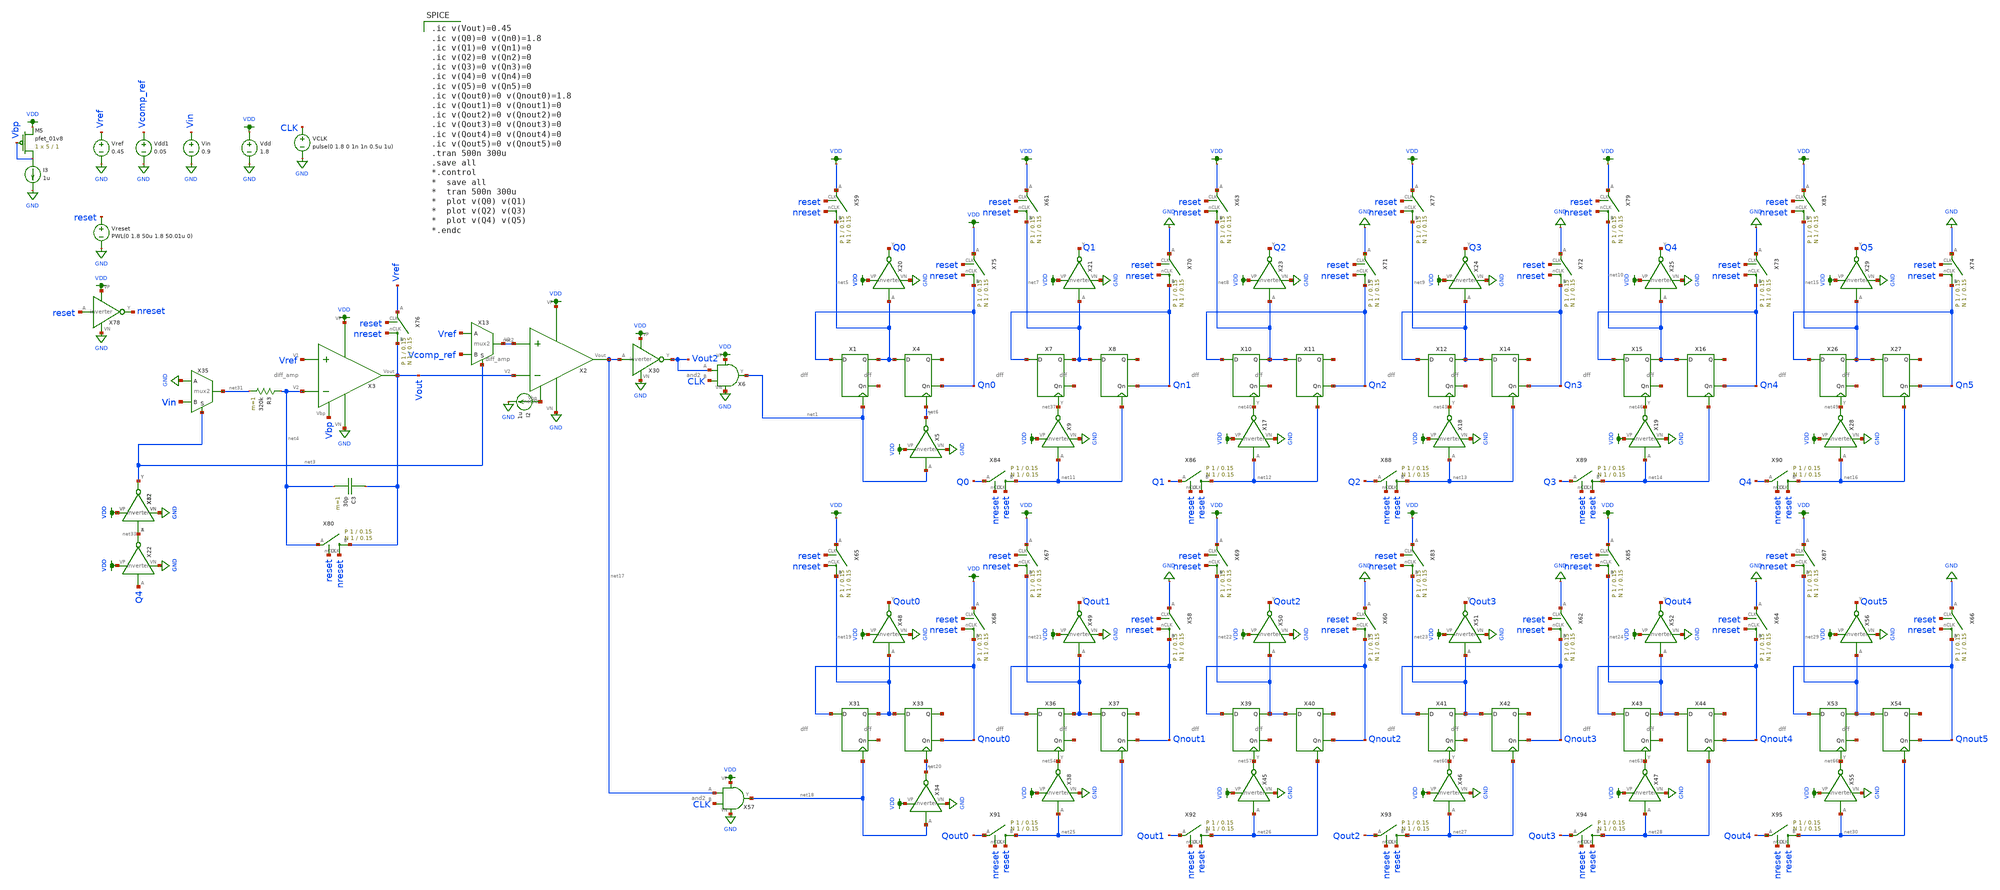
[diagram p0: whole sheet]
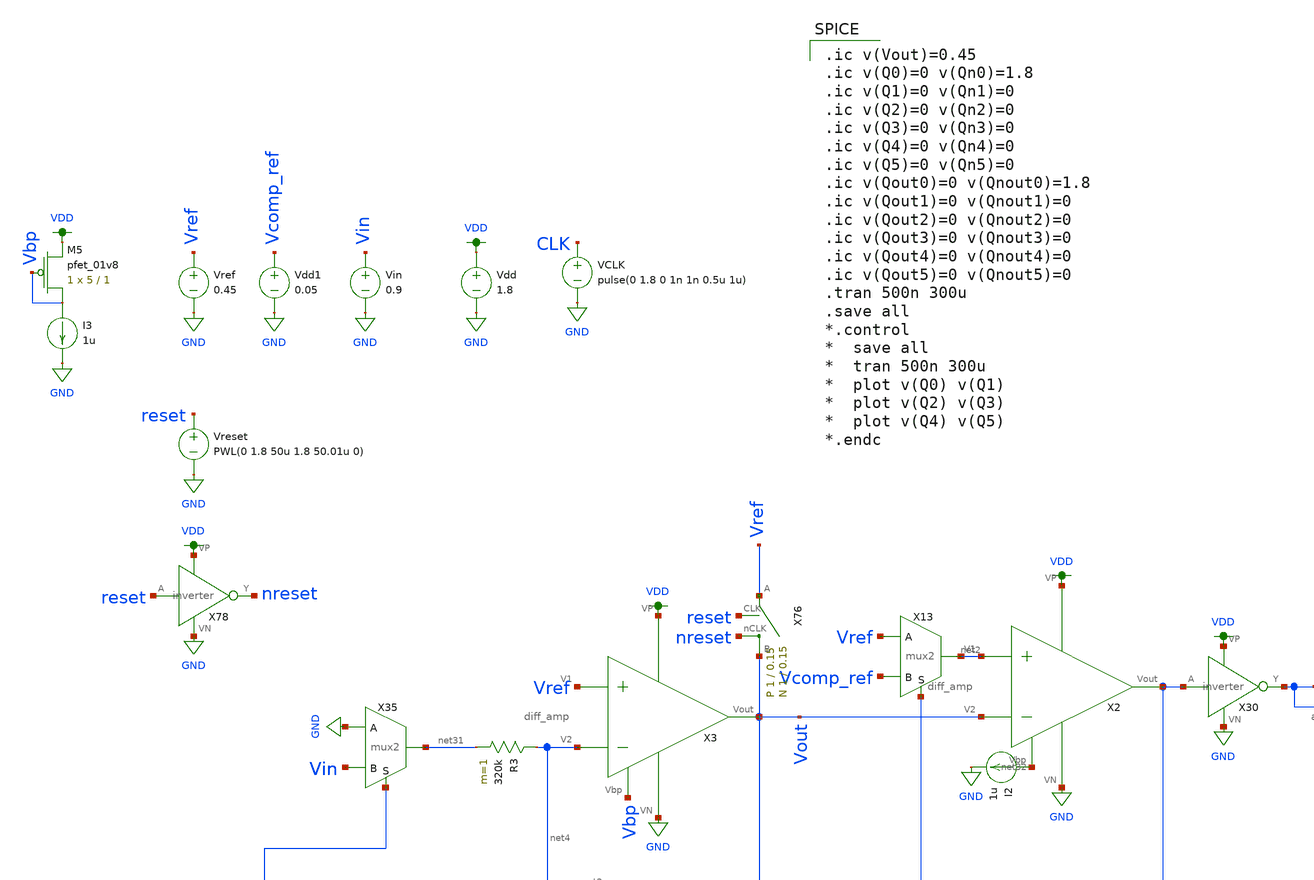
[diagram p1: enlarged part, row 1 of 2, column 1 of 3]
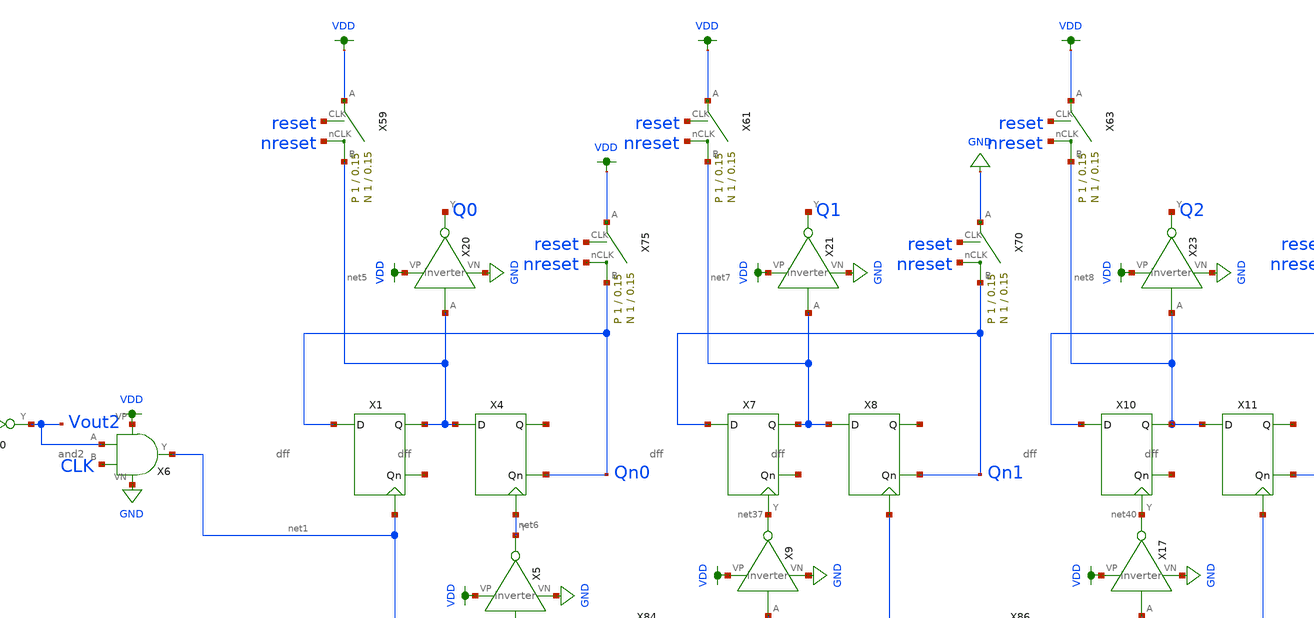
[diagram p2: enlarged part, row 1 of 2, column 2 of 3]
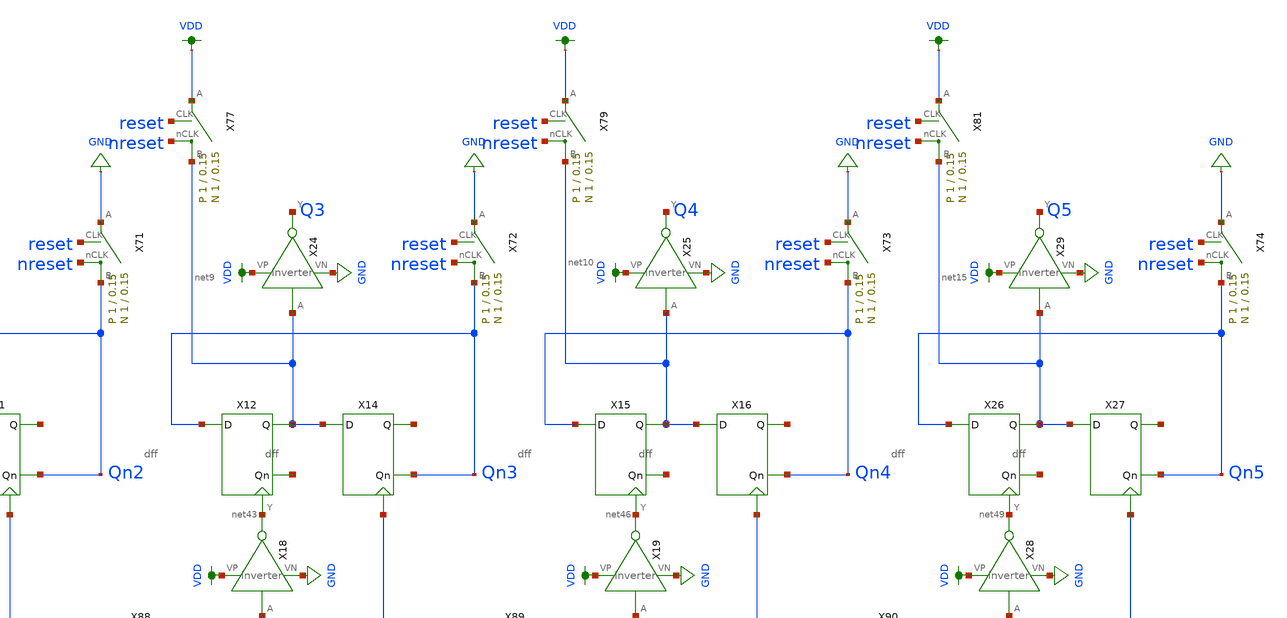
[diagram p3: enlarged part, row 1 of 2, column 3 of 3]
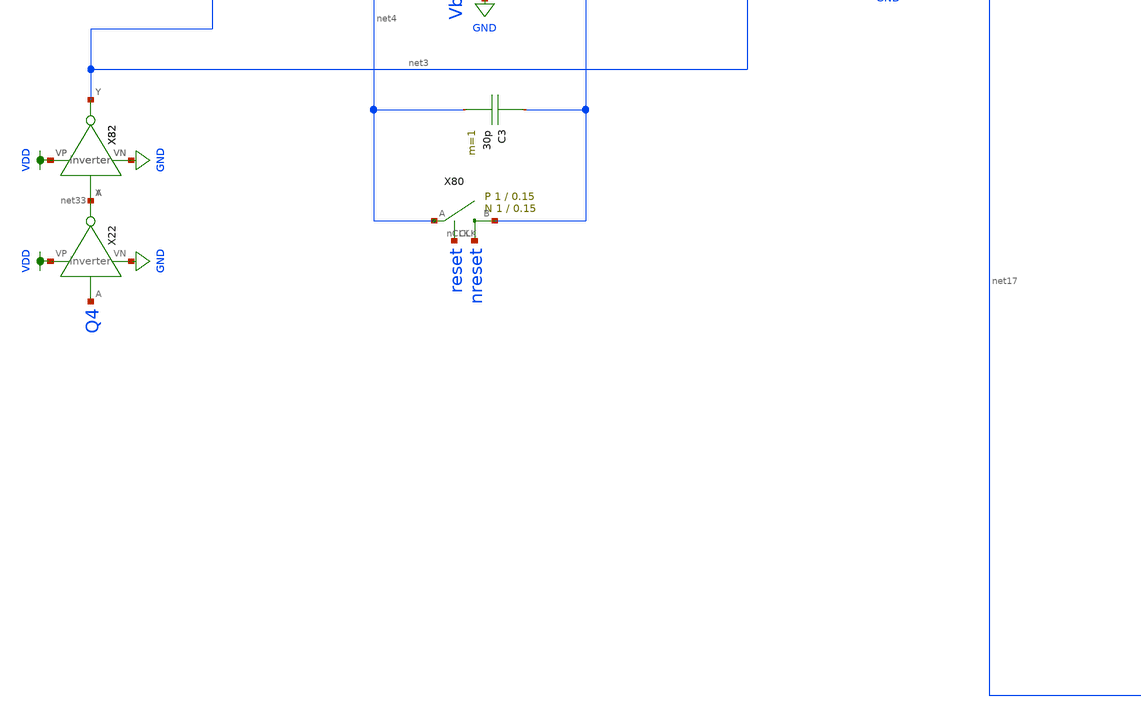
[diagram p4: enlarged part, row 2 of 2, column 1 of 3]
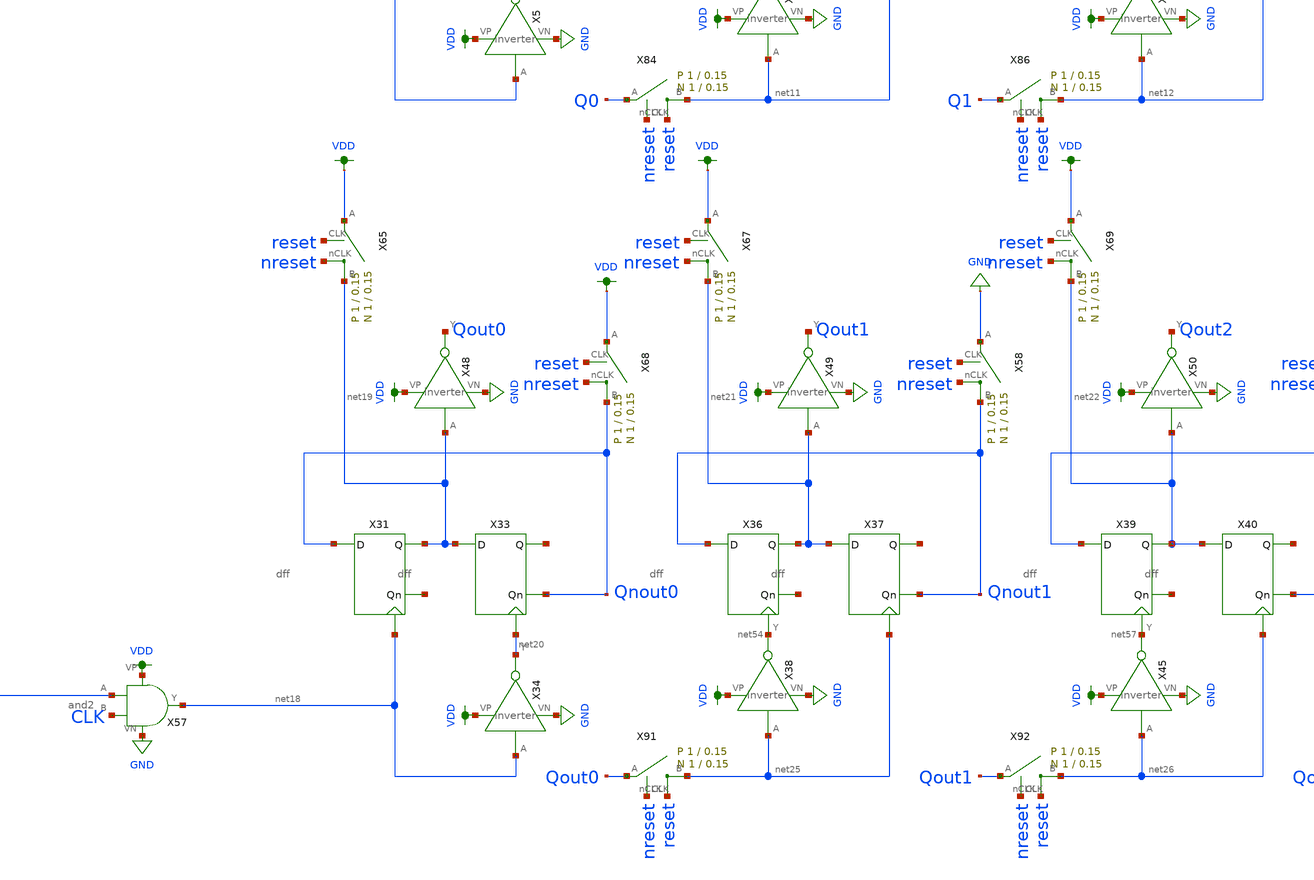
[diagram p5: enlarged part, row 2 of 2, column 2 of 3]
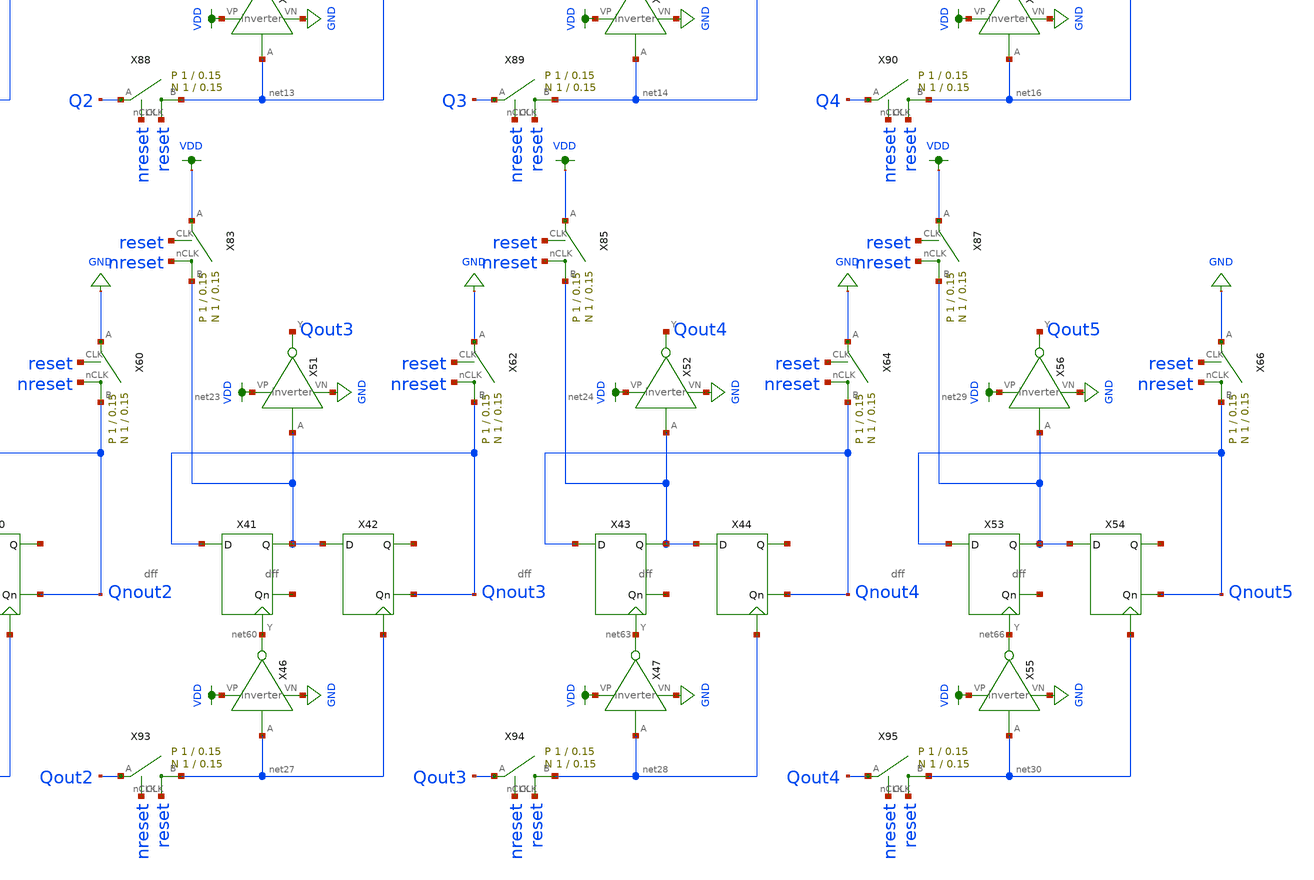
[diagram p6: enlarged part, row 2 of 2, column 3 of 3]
** sch_path: schematic/archive/double-slope-works.sch
**.subckt double-slope-works
X2 VDD net32 net17 net2 Vout GND diff_amp
Vdd VDD GND 1.8
VCLK CLK GND pulse(0 1.8 0 1n 1n 0.5u 1u)
Vdd1 Vcomp_ref GND 0.05
Vin Vin GND 0.9
I2 net32 GND 1u
X6 VDD Vout2 GND net1 CLK and2
X13 net2 Vref Vcomp_ref net3 mux2
X22 Q4 net33 VDD GND inverter
X32 net33 net3 VDD GND inverter
X35 net31 GND Vin net3 mux2
XM5 Vbp Vbp VDD VDD sky130_fd_pr__pfet_01v8 L=1 W=5 nf=1 ad='int((nf+1)/2) * W/nf * 0.29' as='int((nf+2)/2) * W/nf * 0.29'
+ pd='2*int((nf+1)/2) * (W/nf + 0.29)' ps='2*int((nf+2)/2) * (W/nf + 0.29)' nrd='0.29 / W' nrs='0.29 / W'
+ sa=0 sb=0 sd=0 mult=1 m=1
I3 Vbp GND 1u
C3 Vout net4 30p m=1
X3 VDD Vbp Vout Vref net4 GND diff_amp
R3 net4 net31 320k m=1
Vref Vref GND 0.45
X1 Qn0 net34 net5 net1 dff
X4 net5 Qn0 net35 net6 dff
X5 net1 net6 VDD GND inverter
X7 Qn1 net36 net7 net37 dff
X8 net7 Qn1 net38 net11 dff
X9 net11 net37 VDD GND inverter
X10 Qn2 net39 net8 net40 dff
X11 net8 Qn2 net41 net12 dff
X12 Qn3 net42 net9 net43 dff
X14 net9 Qn3 net44 net13 dff
X15 Qn4 net45 net10 net46 dff
X16 net10 Qn4 net47 net14 dff
X17 net12 net40 VDD GND inverter
X18 net13 net43 VDD GND inverter
X19 net14 net46 VDD GND inverter
X20 net5 Q0 VDD GND inverter
X21 net7 Q1 VDD GND inverter
X23 net8 Q2 VDD GND inverter
X24 net9 Q3 VDD GND inverter
X25 net10 Q4 VDD GND inverter
X26 Qn5 net48 net15 net49 dff
X27 net15 Qn5 net50 net16 dff
X28 net16 net49 VDD GND inverter
X29 net15 Q5 VDD GND inverter
X30 net17 Vout2 VDD GND inverter
X31 Qnout0 net51 net19 net18 dff
X33 net19 Qnout0 net52 net20 dff
X34 net18 net20 VDD GND inverter
X36 Qnout1 net53 net21 net54 dff
X37 net21 Qnout1 net55 net25 dff
X38 net25 net54 VDD GND inverter
X39 Qnout2 net56 net22 net57 dff
X40 net22 Qnout2 net58 net26 dff
X41 Qnout3 net59 net23 net60 dff
X42 net23 Qnout3 net61 net27 dff
X43 Qnout4 net62 net24 net63 dff
X44 net24 Qnout4 net64 net28 dff
X45 net26 net57 VDD GND inverter
X46 net27 net60 VDD GND inverter
X47 net28 net63 VDD GND inverter
X48 net19 Qout0 VDD GND inverter
X49 net21 Qout1 VDD GND inverter
X50 net22 Qout2 VDD GND inverter
X51 net23 Qout3 VDD GND inverter
X52 net24 Qout4 VDD GND inverter
X53 Qnout5 net65 net29 net66 dff
X54 net29 Qnout5 net67 net30 dff
X55 net30 net66 VDD GND inverter
X56 net29 Qout5 VDD GND inverter
X57 VDD net17 GND net18 CLK and2
X70 Qn1 GND reset nreset switch Wp=1 Lp=0.15 WW=1 LL=0.15
X71 Qn2 GND reset nreset switch Wp=1 Lp=0.15 WW=1 LL=0.15
X72 Qn3 GND reset nreset switch Wp=1 Lp=0.15 WW=1 LL=0.15
X73 Qn4 GND reset nreset switch Wp=1 Lp=0.15 WW=1 LL=0.15
X74 Qn5 GND reset nreset switch Wp=1 Lp=0.15 WW=1 LL=0.15
X75 Qn0 VDD reset nreset switch Wp=1 Lp=0.15 WW=1 LL=0.15
X59 net5 VDD reset nreset switch Wp=1 Lp=0.15 WW=1 LL=0.15
X61 net7 VDD reset nreset switch Wp=1 Lp=0.15 WW=1 LL=0.15
X63 net8 VDD reset nreset switch Wp=1 Lp=0.15 WW=1 LL=0.15
X77 net9 VDD reset nreset switch Wp=1 Lp=0.15 WW=1 LL=0.15
X79 net10 VDD reset nreset switch Wp=1 Lp=0.15 WW=1 LL=0.15
X81 net15 VDD reset nreset switch Wp=1 Lp=0.15 WW=1 LL=0.15
X65 net19 VDD reset nreset switch Wp=1 Lp=0.15 WW=1 LL=0.15
X67 net21 VDD reset nreset switch Wp=1 Lp=0.15 WW=1 LL=0.15
X69 net22 VDD reset nreset switch Wp=1 Lp=0.15 WW=1 LL=0.15
X83 net23 VDD reset nreset switch Wp=1 Lp=0.15 WW=1 LL=0.15
X85 net24 VDD reset nreset switch Wp=1 Lp=0.15 WW=1 LL=0.15
X87 net29 VDD reset nreset switch Wp=1 Lp=0.15 WW=1 LL=0.15
X58 Qnout1 GND reset nreset switch Wp=1 Lp=0.15 WW=1 LL=0.15
X60 Qnout2 GND reset nreset switch Wp=1 Lp=0.15 WW=1 LL=0.15
X62 Qnout3 GND reset nreset switch Wp=1 Lp=0.15 WW=1 LL=0.15
X64 Qnout4 GND reset nreset switch Wp=1 Lp=0.15 WW=1 LL=0.15
X66 Qnout5 GND reset nreset switch Wp=1 Lp=0.15 WW=1 LL=0.15
X68 Qnout0 VDD reset nreset switch Wp=1 Lp=0.15 WW=1 LL=0.15
X76 Vout Vref reset nreset switch Wp=1 Lp=0.15 WW=1 LL=0.15
Vreset reset GND PWL(0 1.8 50u 1.8 50.01u 0)
X78 reset nreset VDD GND inverter
X80 Vout net4 reset nreset switch Wp=1 Lp=0.15 WW=1 LL=0.15
X82 net33 net3 VDD GND inverter
X84 net11 Q0 nreset reset switch Wp=1 Lp=0.15 WW=1 LL=0.15
X86 net12 Q1 nreset reset switch Wp=1 Lp=0.15 WW=1 LL=0.15
X88 net13 Q2 nreset reset switch Wp=1 Lp=0.15 WW=1 LL=0.15
X89 net14 Q3 nreset reset switch Wp=1 Lp=0.15 WW=1 LL=0.15
X90 net16 Q4 nreset reset switch Wp=1 Lp=0.15 WW=1 LL=0.15
X91 net25 Qout0 nreset reset switch Wp=1 Lp=0.15 WW=1 LL=0.15
X92 net26 Qout1 nreset reset switch Wp=1 Lp=0.15 WW=1 LL=0.15
X93 net27 Qout2 nreset reset switch Wp=1 Lp=0.15 WW=1 LL=0.15
X94 net28 Qout3 nreset reset switch Wp=1 Lp=0.15 WW=1 LL=0.15
X95 net30 Qout4 nreset reset switch Wp=1 Lp=0.15 WW=1 LL=0.15
**** begin user architecture code

.ic v(Vout)=0.45
.ic v(Q0)=0 v(Qn0)=1.8
.ic v(Q1)=0 v(Qn1)=0
.ic v(Q2)=0 v(Qn2)=0
.ic v(Q3)=0 v(Qn3)=0
.ic v(Q4)=0 v(Qn4)=0
.ic v(Q5)=0 v(Qn5)=0
.ic v(Qout0)=0 v(Qnout0)=1.8
.ic v(Qout1)=0 v(Qnout1)=0
.ic v(Qout2)=0 v(Qnout2)=0
.ic v(Qout3)=0 v(Qnout3)=0
.ic v(Qout4)=0 v(Qnout4)=0
.ic v(Qout5)=0 v(Qnout5)=0
.tran 500n 300u
.save all
*.control
*  save all
*  tran 500n 300u
*  plot v(Q0) v(Q1)
*  plot v(Q2) v(Q3)
*  plot v(Q4) v(Q5)
*.endc


.option wnflag=1
.param MC_SWITCH=0.0
.lib ~/skywater/skywater-pdk/libraries/sky130_fd_pr_ngspice/latest/models/sky130.lib.spice tt

**** end user architecture code
**.ends
.GLOBAL GND
.GLOBAL VDD
.end
